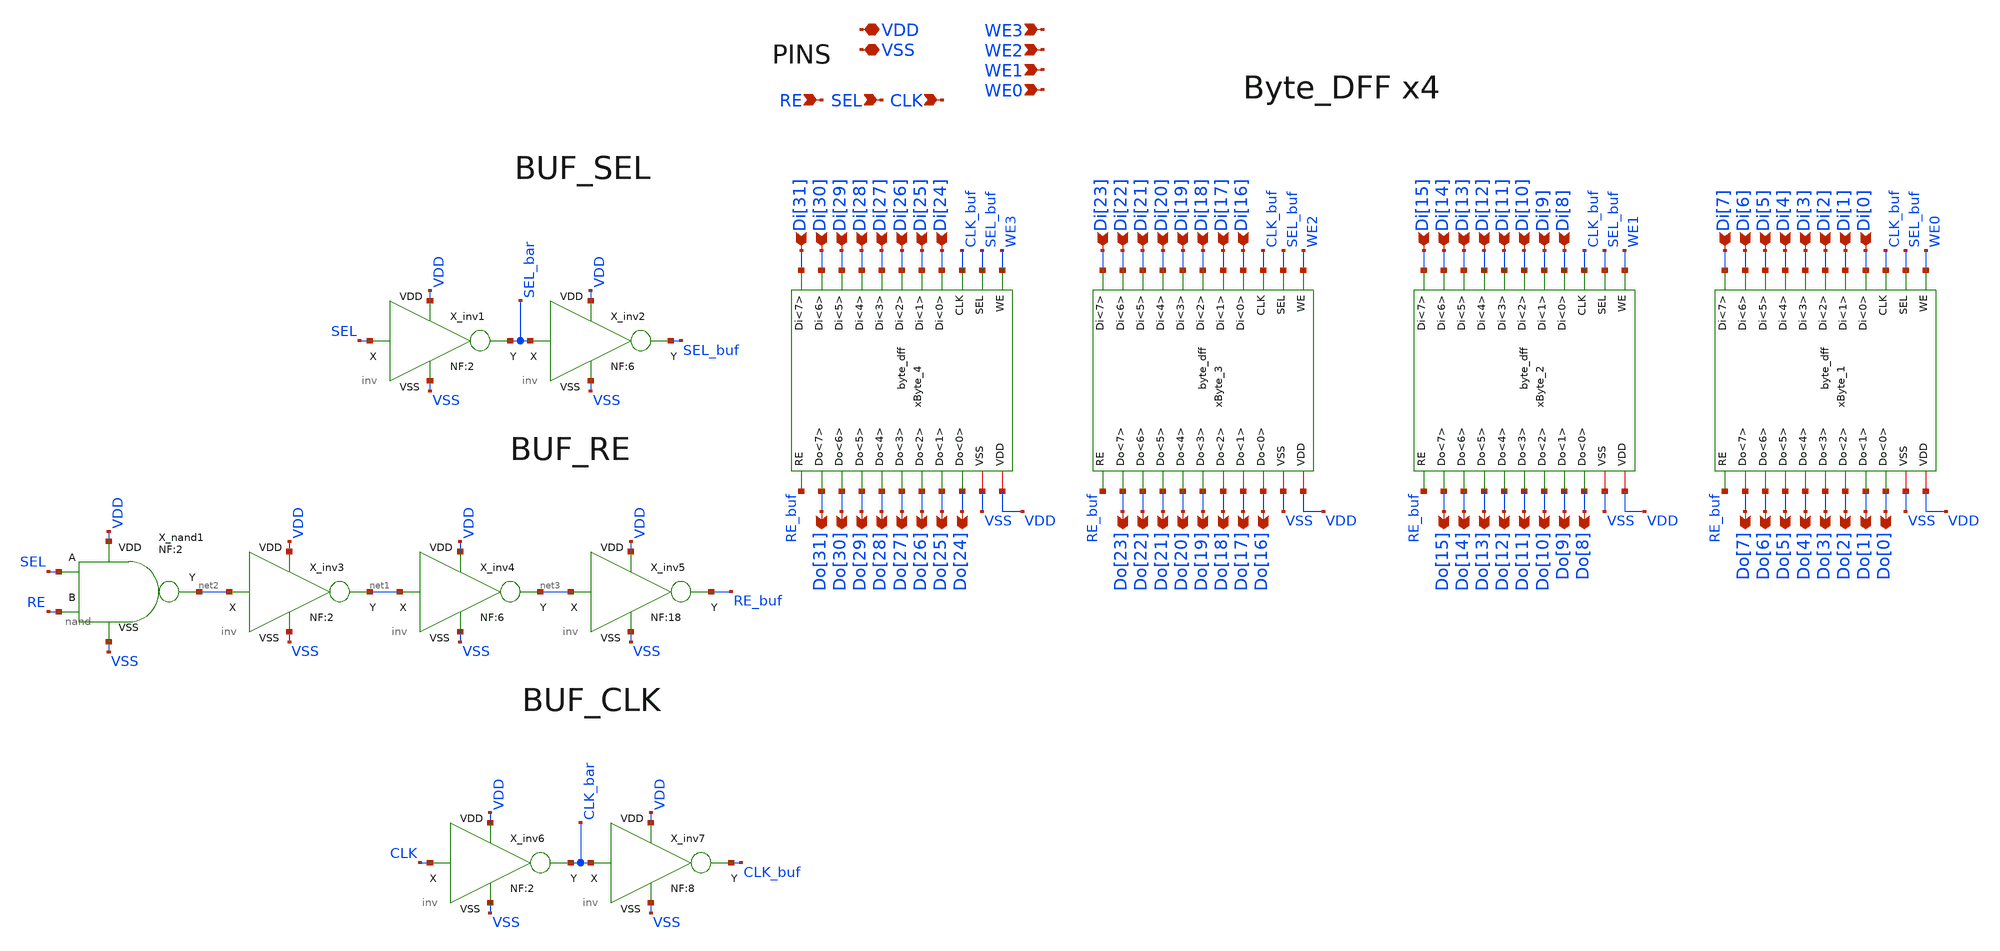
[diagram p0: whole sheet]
** sch_path: xschem_lib/DFFRAM_full_custom/word.sch
**.subckt word SEL WE0 Di[31] Di[30] Di[29] Di[28] Di[27] Di[26] Di[25] Di[24] Do[31] Do[30] Do[29]
*+ Do[28] Do[27] Do[26] Do[25] Do[24] VDD VSS Di[23] Di[22] Di[21] Di[20] Di[19] Di[18] Di[17] Di[16] Do[23]
*+ Do[22] Do[21] Do[20] Do[19] Do[18] Do[17] Do[16] Di[15] Di[14] Di[13] Di[12] Di[11] Di[10] Di[9] Di[8]
*+ Do[15] Do[14] Do[13] Do[12] Do[11] Do[10] Do[9] Do[8] Di[7] Di[6] Di[5] Di[4] Di[3] Di[2] Di[1] Di[0]
*+ Do[7] Do[6] Do[5] Do[4] Do[3] Do[2] Do[1] Do[0] WE1 WE2 WE3 CLK RE
*.ipin SEL
*.ipin WE0
*.ipin Di[31]
*.ipin Di[30]
*.ipin Di[29]
*.ipin Di[28]
*.ipin Di[27]
*.ipin Di[26]
*.ipin Di[25]
*.ipin Di[24]
*.opin Do[31]
*.opin Do[30]
*.opin Do[29]
*.opin Do[28]
*.opin Do[27]
*.opin Do[26]
*.opin Do[25]
*.opin Do[24]
*.iopin VDD
*.iopin VSS
*.ipin Di[23]
*.ipin Di[22]
*.ipin Di[21]
*.ipin Di[20]
*.ipin Di[19]
*.ipin Di[18]
*.ipin Di[17]
*.ipin Di[16]
*.opin Do[23]
*.opin Do[22]
*.opin Do[21]
*.opin Do[20]
*.opin Do[19]
*.opin Do[18]
*.opin Do[17]
*.opin Do[16]
*.ipin Di[15]
*.ipin Di[14]
*.ipin Di[13]
*.ipin Di[12]
*.ipin Di[11]
*.ipin Di[10]
*.ipin Di[9]
*.ipin Di[8]
*.opin Do[15]
*.opin Do[14]
*.opin Do[13]
*.opin Do[12]
*.opin Do[11]
*.opin Do[10]
*.opin Do[9]
*.opin Do[8]
*.ipin Di[7]
*.ipin Di[6]
*.ipin Di[5]
*.ipin Di[4]
*.ipin Di[3]
*.ipin Di[2]
*.ipin Di[1]
*.ipin Di[0]
*.opin Do[7]
*.opin Do[6]
*.opin Do[5]
*.opin Do[4]
*.opin Do[3]
*.opin Do[2]
*.opin Do[1]
*.opin Do[0]
*.ipin WE1
*.ipin WE2
*.ipin WE3
*.ipin CLK
*.ipin RE
xByte_1 VDD VSS WE0 Di[3] Di[7] Do[3] Do[7] CLK_buf SEL_buf Di[2] Di[6] Do[2] Do[6] Di[5] Di[1]
+ Do[5] Do[1] Di[4] Do[4] Di[0] Do[0] RE_buf byte_dff NF=NF
X_inv1 SEL VDD VSS SEL_bar inv NF=2
X_inv2 SEL_bar VDD VSS SEL_buf inv NF=6
xByte_2 VDD VSS WE1 Di[11] Di[15] Do[11] Do[15] CLK_buf SEL_buf Di[10] Di[14] Do[10] Do[14] Di[13]
+ Di[9] Do[13] Do[9] Di[12] Do[12] Di[8] Do[8] RE_buf byte_dff NF=NF
xByte_3 VDD VSS WE2 Di[19] Di[23] Do[19] Do[23] CLK_buf SEL_buf Di[18] Di[22] Do[18] Do[22] Di[21]
+ Di[17] Do[21] Do[17] Di[20] Do[20] Di[16] Do[16] RE_buf byte_dff NF=NF
xByte_4 VDD VSS WE3 Di[27] Di[31] Do[27] Do[31] CLK_buf SEL_buf Di[26] Di[30] Do[26] Do[30] Di[29]
+ Di[25] Do[29] Do[25] Di[28] Do[28] Di[24] Do[24] RE_buf byte_dff NF=NF
X_nand1 RE SEL net2 VDD VSS nand NF=2
X_inv3 net2 VDD VSS net1 inv NF=2
X_inv4 net1 VDD VSS net3 inv NF=6
X_inv5 net3 VDD VSS RE_buf inv NF=18
X_inv6 CLK VDD VSS CLK_bar inv NF=2
X_inv7 CLK_bar VDD VSS CLK_buf inv NF=8
**.ends
.end
